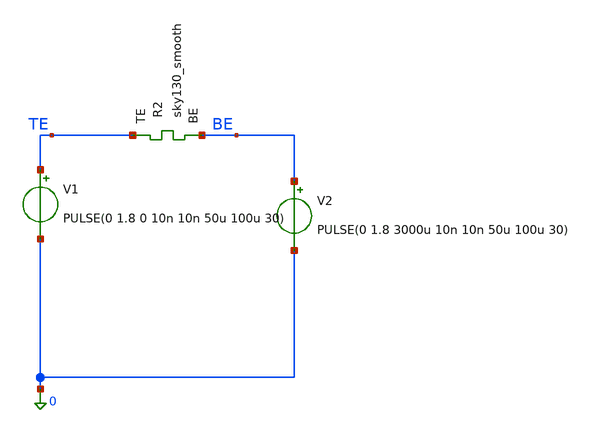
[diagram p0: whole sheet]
** sch_path: memristor_models/sky130_smooth/tb_1R_smooth.sch
**.subckt tb_1R_smooth
V1 TE 0 PULSE(0 1.8 0 10n 10n 50u 100u 30)
XR2 TE BE sky130_smooth Tfilament_0=3.3e-9
V2 BE 0 PULSE(0 1.8 3000u 10n 10n 50u 100u 30)
**** begin user architecture code

** opencircuitdesign pdks install
.inc $::SKYWATER_MODELS/sky130_smooth.spice



.option savecurrents
.tran 1u 6000u
.control
	save all
	run
	write tb_1R_smooth.raw
.endc



**** end user architecture code
**.ends
.end
